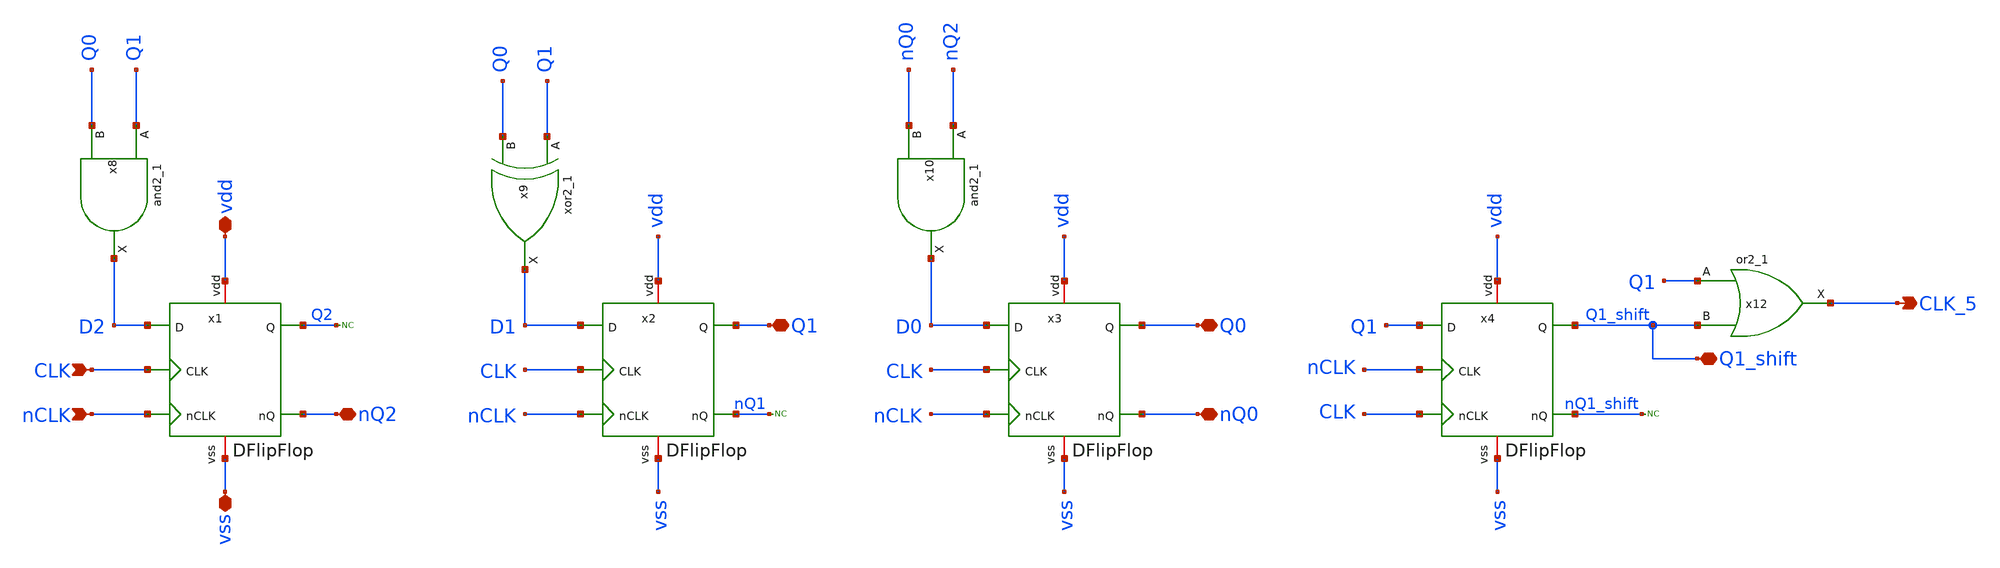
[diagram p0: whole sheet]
** sch_path: xschem/div_by_5.sch
**.subckt div_by_5 vdd vss CLK CLK_5 nCLK nQ2 Q1 Q0 nQ0 Q1_shift
*.iopin vdd
*.iopin vss
*.ipin CLK
*.opin CLK_5
*.ipin nCLK
*.iopin nQ2
*.iopin Q1
*.iopin Q0
*.iopin nQ0
*.iopin Q1_shift
x8 Q1 Q0 vss vss vdd vdd D2 sky130_fd_sc_hs__and2_1
x9 Q1 Q0 vss vss vdd vdd D1 sky130_fd_sc_hs__xor2_1
x10 nQ2 nQ0 vss vss vdd vdd D0 sky130_fd_sc_hs__and2_1
x12 Q1 Q1_shift vss vss vdd vdd CLK_5 sky130_fd_sc_hs__or2_1
x1 vdd Q2 nQ2 vss D2 CLK nCLK DFlipFlop
x2 vdd Q1 nQ1 vss D1 CLK nCLK DFlipFlop
x3 vdd Q0 nQ0 vss D0 CLK nCLK DFlipFlop
x4 vdd Q1_shift nQ1_shift vss Q1 nCLK CLK DFlipFlop
* noconn nQ1
* noconn nQ1_shift
* noconn Q2
**.ends
.end
